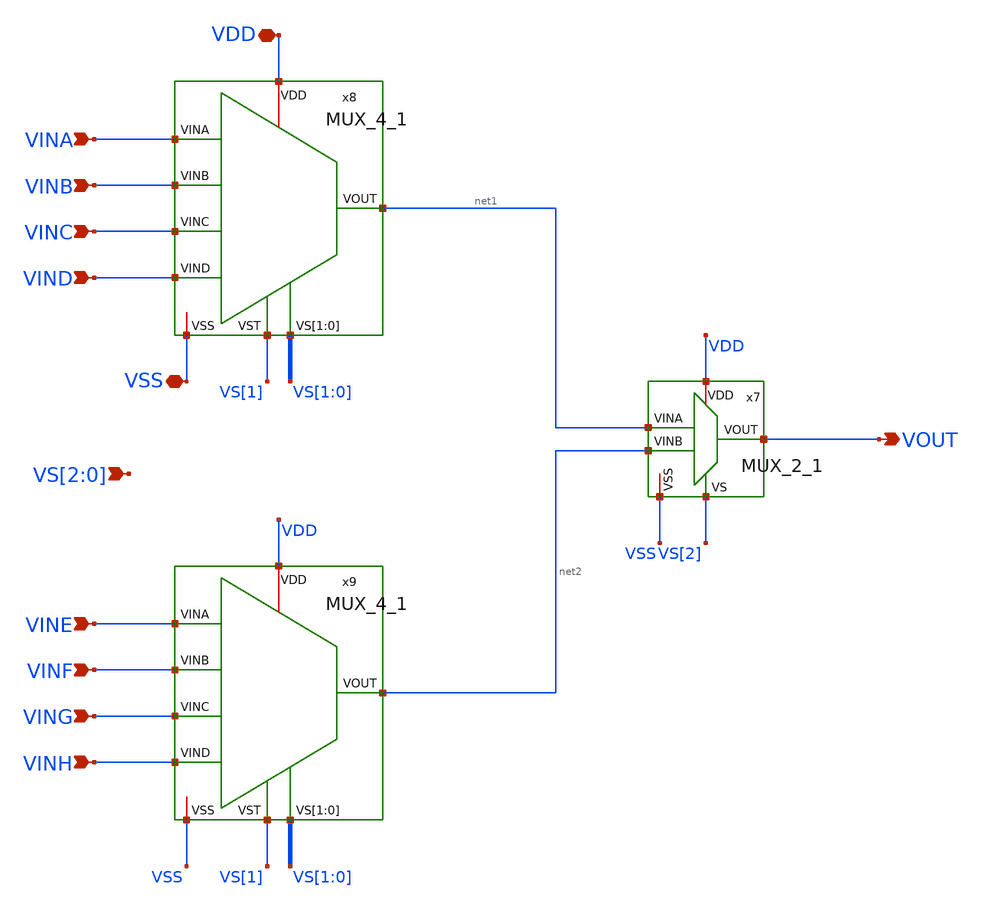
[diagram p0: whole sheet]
** sch_path: std_cells/MUX_8_1.sch
**.subckt MUX_8_1 VSS VOUT VDD VINA VINB VINC VIND VS[2],VS[1],VS[0] VINE VINF VING VINH
*.iopin VSS
*.opin VOUT
*.iopin VDD
*.ipin VINA
*.ipin VINB
*.ipin VINC
*.ipin VIND
*.ipin VS[2],VS[1],VS[0]
*.ipin VINE
*.ipin VINF
*.ipin VING
*.ipin VINH
x7 VDD net1 VOUT VS[2] net2 VSS MUX_2_1
x8 VINA VINB VDD net1 VS[1] VS[0] VINC VSS VIND VS[1] MUX_4_1
x9 VINE VINF VDD net2 VS[1] VS[0] VING VSS VINH VS[1] MUX_4_1
**.ends
.end
